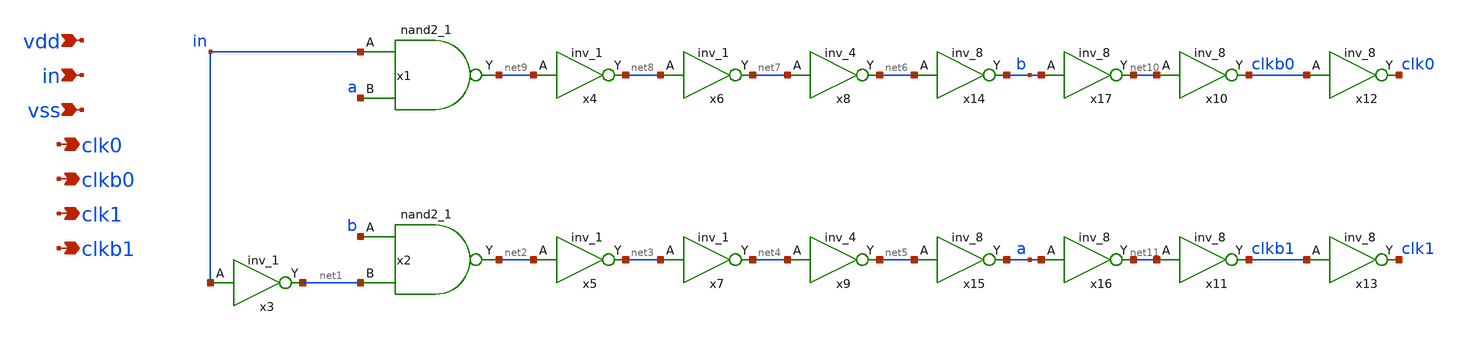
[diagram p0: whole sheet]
** sch_path: xschem/nooverlap_clk.sch
**.subckt nooverlap_clk vdd in vss clk0 clkb0 clk1 clkb1
*.ipin vdd
*.ipin in
*.ipin vss
*.opin clk0
*.opin clkb0
*.opin clk1
*.opin clkb1
x1 in a vss vss vdd vdd net9 sky130_fd_sc_hd__nand2_1
x2 b net1 vss vss vdd vdd net2 sky130_fd_sc_hd__nand2_1
x3 in vss vss vdd vdd net1 sky130_fd_sc_hd__inv_1
x4 net9 vss vss vdd vdd net8 sky130_fd_sc_hd__inv_1
x5 net2 vss vss vdd vdd net3 sky130_fd_sc_hd__inv_1
x6 net8 vss vss vdd vdd net7 sky130_fd_sc_hd__inv_1
x7 net3 vss vss vdd vdd net4 sky130_fd_sc_hd__inv_1
x8 net7 vss vss vdd vdd net6 sky130_fd_sc_hd__inv_4
x9 net4 vss vss vdd vdd net5 sky130_fd_sc_hd__inv_4
x10 net10 vss vss vdd vdd clkb0 sky130_fd_sc_hd__inv_8
x11 net11 vss vss vdd vdd clkb1 sky130_fd_sc_hd__inv_8
x12 clkb0 vss vss vdd vdd clk0 sky130_fd_sc_hd__inv_8
x13 clkb1 vss vss vdd vdd clk1 sky130_fd_sc_hd__inv_8
x14 net6 vss vss vdd vdd b sky130_fd_sc_hd__inv_8
x15 net5 vss vss vdd vdd a sky130_fd_sc_hd__inv_8
x16 a vss vss vdd vdd net11 sky130_fd_sc_hd__inv_8
x17 b vss vss vdd vdd net10 sky130_fd_sc_hd__inv_8
**.ends
.end
